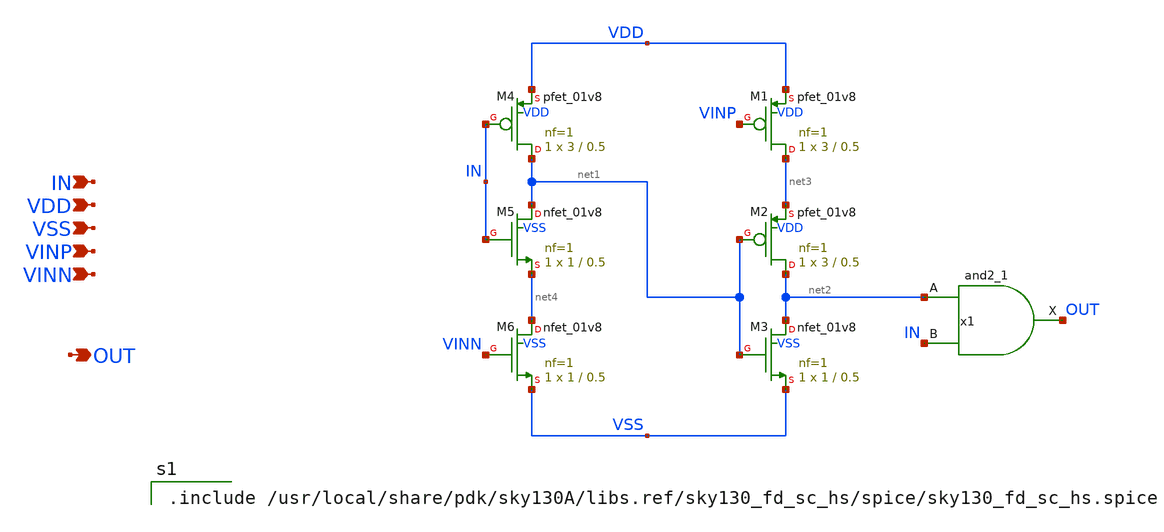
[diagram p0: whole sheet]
** sch_path: xschem/delay_gate_ori.sch
**.subckt delay_gate_ori VINP VINN IN VSS VDD OUT
*.ipin VINP
*.ipin VINN
*.ipin IN
*.ipin VSS
*.ipin VDD
*.opin OUT
XM1 net3 VINP VDD VDD sky130_fd_pr__pfet_01v8 L=0.5 W=3 nf=1 ad='int((nf+1)/2) * W/nf * 0.29' as='int((nf+2)/2) * W/nf * 0.29'
+ pd='2*int((nf+1)/2) * (W/nf + 0.29)' ps='2*int((nf+2)/2) * (W/nf + 0.29)' nrd='0.29 / W' nrs='0.29 / W'
+ sa=0 sb=0 sd=0 mult=1 m=1
XM2 net2 net1 net3 VDD sky130_fd_pr__pfet_01v8 L=0.5 W=3 nf=1 ad='int((nf+1)/2) * W/nf * 0.29' as='int((nf+2)/2) * W/nf * 0.29'
+ pd='2*int((nf+1)/2) * (W/nf + 0.29)' ps='2*int((nf+2)/2) * (W/nf + 0.29)' nrd='0.29 / W' nrs='0.29 / W'
+ sa=0 sb=0 sd=0 mult=1 m=1
XM3 net2 net1 VSS VSS sky130_fd_pr__nfet_01v8 L=0.5 W=1 nf=1 ad='int((nf+1)/2) * W/nf * 0.29' as='int((nf+2)/2) * W/nf * 0.29'
+ pd='2*int((nf+1)/2) * (W/nf + 0.29)' ps='2*int((nf+2)/2) * (W/nf + 0.29)' nrd='0.29 / W' nrs='0.29 / W'
+ sa=0 sb=0 sd=0 mult=1 m=1
XM4 net1 IN VDD VDD sky130_fd_pr__pfet_01v8 L=0.5 W=3 nf=1 ad='int((nf+1)/2) * W/nf * 0.29' as='int((nf+2)/2) * W/nf * 0.29'
+ pd='2*int((nf+1)/2) * (W/nf + 0.29)' ps='2*int((nf+2)/2) * (W/nf + 0.29)' nrd='0.29 / W' nrs='0.29 / W'
+ sa=0 sb=0 sd=0 mult=1 m=1
XM5 net1 IN net4 VSS sky130_fd_pr__nfet_01v8 L=0.5 W=1 nf=1 ad='int((nf+1)/2) * W/nf * 0.29' as='int((nf+2)/2) * W/nf * 0.29'
+ pd='2*int((nf+1)/2) * (W/nf + 0.29)' ps='2*int((nf+2)/2) * (W/nf + 0.29)' nrd='0.29 / W' nrs='0.29 / W'
+ sa=0 sb=0 sd=0 mult=1 m=1
XM6 net4 VINN VSS VSS sky130_fd_pr__nfet_01v8 L=0.5 W=1 nf=1 ad='int((nf+1)/2) * W/nf * 0.29' as='int((nf+2)/2) * W/nf * 0.29'
+ pd='2*int((nf+1)/2) * (W/nf + 0.29)' ps='2*int((nf+2)/2) * (W/nf + 0.29)' nrd='0.29 / W' nrs='0.29 / W'
+ sa=0 sb=0 sd=0 mult=1 m=1
x1 net2 IN VSS VSS VDD VDD OUT sky130_fd_sc_hs__and2_1
**** begin user architecture code

.include /usr/local/share/pdk/sky130A/libs.ref/sky130_fd_sc_hs/spice/sky130_fd_sc_hs.spice

**** end user architecture code
**.ends
.end
